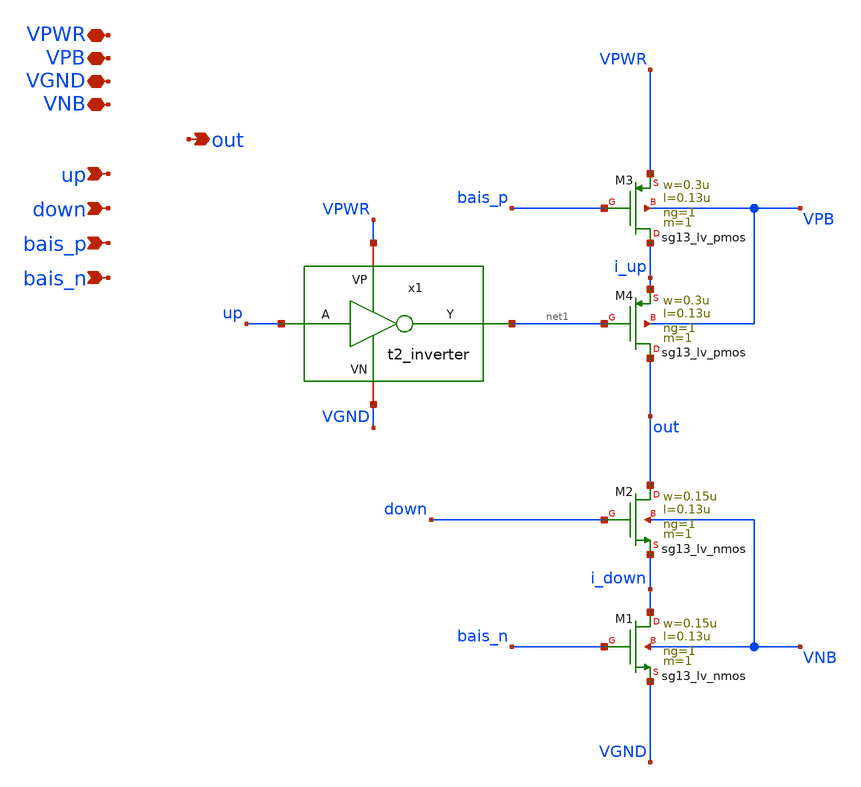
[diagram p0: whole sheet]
** sch_path: Team 2 Design/design_data/xschem/t2_charge_pump.sch
**.subckt t2_charge_pump VPWR up out VPB VGND VNB down bais_p bais_n
*.iopin VPWR
*.ipin up
*.opin out
*.iopin VPB
*.iopin VGND
*.iopin VNB
*.ipin down
*.ipin bais_p
*.ipin bais_n
XM1 i_down bais_n VGND VNB sg13_lv_nmos w=0.15u l=0.13u ng=1 m=1 mm_ok=1
XM2 out down i_down VNB sg13_lv_nmos w=0.15u l=0.13u ng=1 m=1 mm_ok=1
XM3 i_up bais_p VPWR VPB sg13_lv_pmos w=0.3u l=0.13u ng=1 m=1 mm_ok=1
XM4 out net1 i_up VPB sg13_lv_pmos w=0.3u l=0.13u ng=1 m=1 mm_ok=1
x1 VPWR up net1 VGND t2_inverter
**.ends

* expanding   symbol:  t2_inverter.sym # of pins=4
** sym_path: Team 2 Design/design_data/xschem/t2_inverter.sym
** sch_path: Team 2 Design/design_data/xschem/t2_inverter.sch
.subckt t2_inverter VP A Y VN
*.iopin VP
*.iopin VN
*.ipin A
*.opin Y
XM2 Y A VP VP sg13_lv_pmos w=0.3u l=0.13u ng=1 m=1 mm_ok=1
XM1 Y A VN VN sg13_lv_nmos w=0.15u l=0.13u ng=1 m=1 mm_ok=1
.ends

.end
